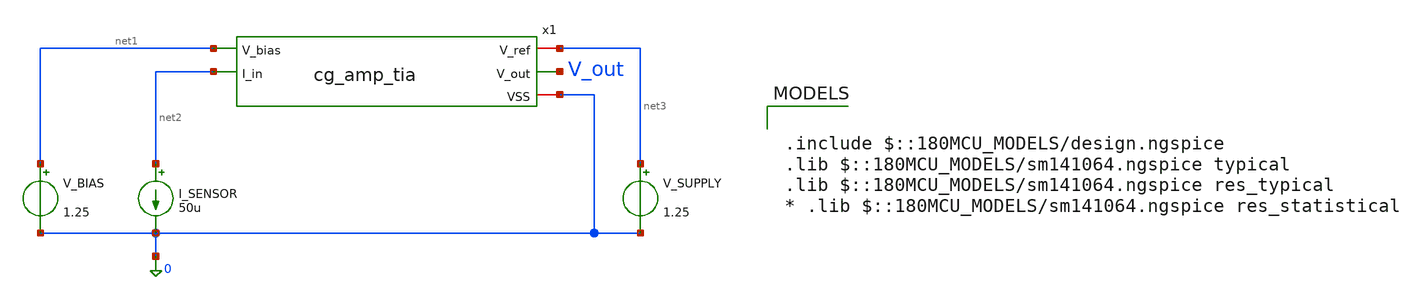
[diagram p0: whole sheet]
** sch_path: schematics/tb_cg_amp_tia.sch
**.subckt tb_cg_amp_tia
x1 net3 V_out net1 net2 0 cg_amp_tia
V_SUPPLY net3 0 1.25
V_BIAS net1 0 1.25
I_SENSOR net2 0 50u
**** begin user architecture code

.include $::180MCU_MODELS/design.ngspice
.lib $::180MCU_MODELS/sm141064.ngspice typical
.lib $::180MCU_MODELS/sm141064.ngspice res_typical
* .lib $::180MCU_MODELS/sm141064.ngspice res_statistical



.control
  op
  print v(V_out)
  print @m.x1.xm1.m0[vgs] @m.x1.xm1.m0[vth] @m.x1.xm1.m0[vdsat] @m.x1.xm1.m0[id] @m.x1.xm1.m0[gm]
+ @m.x1.xm1.m0[gds]
  print @r.x1.xr1.rt1[resistance] @r.x1.xr1.rt2[resistance]

  dc I_SENSOR 0 50u 1u
  let V_out_swp = v(V_out)
  plot V_out_swp title "CG-TIA: Sensor Current to Voltage"
  wrdata /foss/designs/analog-perceptron-gf180mcu/plots/cg_amp_tia_sweep.txt V_out_swp
  * === OP-SWEEP DIAGNOSTIC: M1 headroom across full 0-50uA input range ===
  save all @m.x1.xm1.m0[vgs] @m.x1.xm1.m0[vth] @m.x1.xm1.m0[vdsat] @m.x1.xm1.m0[id] @m.x1.xm1.m0[gm]
+ @m.x1.xm1.m0[gds]
  dc I_SENSOR 0 50u 1u
  wrdata /foss/designs/analog-perceptron-gf180mcu/plots/opsweep_cg_amp_tia.txt v(V_out)
+ @m.x1.xm1.m0[vgs] @m.x1.xm1.m0[vth] @m.x1.xm1.m0[vdsat] @m.x1.xm1.m0[id] @m.x1.xm1.m0[gm] @m.x1.xm1.m0[gds]
.endc


**** end user architecture code
**.ends

* expanding   symbol:  analog-perceptron-gf180mcu/schematics/cg_amp_tia.sym # of pins=5
** sym_path: schematics/cg_amp_tia.sym
** sch_path: schematics/cg_amp_tia.sch
.subckt cg_amp_tia V_ref V_out V_bias I_in VSS
*.iopin V_ref
*.iopin VSS
*.ipin I_in
*.ipin V_bias
*.opin V_out
XM1 V_out V_bias I_in VSS nfet_03v3 L=0.5u W=10u nf=1 ad='int((nf+1)/2) * W/nf * 0.18u' as='int((nf+2)/2) * W/nf * 0.18u'
+ pd='2*int((nf+1)/2) * (W/nf + 0.18u)' ps='2*int((nf+2)/2) * (W/nf + 0.18u)' nrd='0.18u / W' nrs='0.18u / W'
+ sa=0 sb=0 sd=0 m=1
XR1 V_out V_ref VSS ppolyf_u_1k r_width=1e-6 r_length=2.7e-6 m=1
.ends

.end
